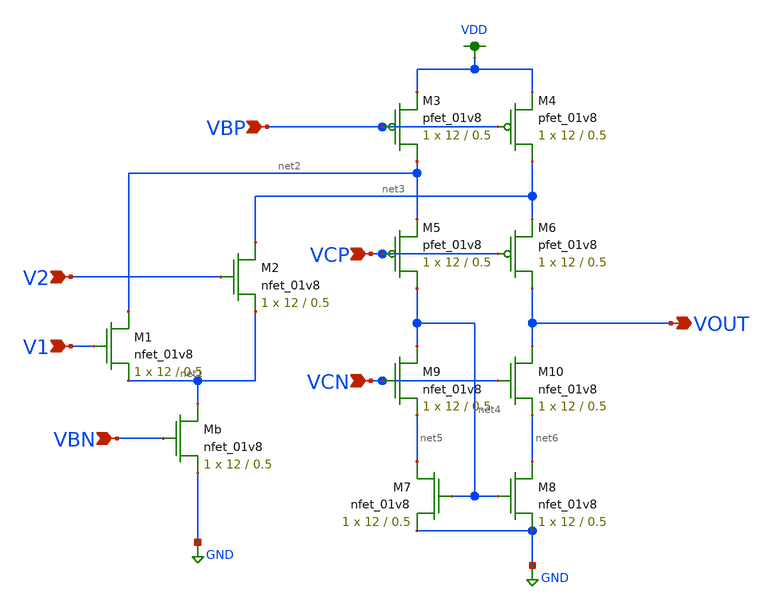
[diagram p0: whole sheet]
** sch_path: MP3/FCDA (copy).sch
**.subckt FCDA (copy) V2 V1 VBN VCN VCP VBP VOUT
*.ipin V2
*.ipin V1
*.ipin VBN
*.ipin VCN
*.ipin VCP
*.ipin VBP
*.opin VOUT
XM1 net2 V1 net1 GND sky130_fd_pr__nfet_01v8 L=0.5 W=12 nf=1 ad='int((nf+1)/2) * W/nf * 0.29' as='int((nf+2)/2) * W/nf * 0.29'
+ pd='2*int((nf+1)/2) * (W/nf + 0.29)' ps='2*int((nf+2)/2) * (W/nf + 0.29)' nrd='0.29 / W' nrs='0.29 / W'
+ sa=0 sb=0 sd=0 mult=1 m=1
XM2 net3 V2 net1 GND sky130_fd_pr__nfet_01v8 L=0.5 W=12 nf=1 ad='int((nf+1)/2) * W/nf * 0.29' as='int((nf+2)/2) * W/nf * 0.29'
+ pd='2*int((nf+1)/2) * (W/nf + 0.29)' ps='2*int((nf+2)/2) * (W/nf + 0.29)' nrd='0.29 / W' nrs='0.29 / W'
+ sa=0 sb=0 sd=0 mult=1 m=1
XM3 net2 VBP VDD VDD sky130_fd_pr__pfet_01v8 L=0.5 W=12 nf=1 ad='int((nf+1)/2) * W/nf * 0.29' as='int((nf+2)/2) * W/nf * 0.29'
+ pd='2*int((nf+1)/2) * (W/nf + 0.29)' ps='2*int((nf+2)/2) * (W/nf + 0.29)' nrd='0.29 / W' nrs='0.29 / W'
+ sa=0 sb=0 sd=0 mult=1 m=1
XM4 net3 VBP VDD VDD sky130_fd_pr__pfet_01v8 L=0.5 W=12 nf=1 ad='int((nf+1)/2) * W/nf * 0.29' as='int((nf+2)/2) * W/nf * 0.29'
+ pd='2*int((nf+1)/2) * (W/nf + 0.29)' ps='2*int((nf+2)/2) * (W/nf + 0.29)' nrd='0.29 / W' nrs='0.29 / W'
+ sa=0 sb=0 sd=0 mult=1 m=1
XM5 net4 VCP net2 VDD sky130_fd_pr__pfet_01v8 L=0.5 W=12 nf=1 ad='int((nf+1)/2) * W/nf * 0.29' as='int((nf+2)/2) * W/nf * 0.29'
+ pd='2*int((nf+1)/2) * (W/nf + 0.29)' ps='2*int((nf+2)/2) * (W/nf + 0.29)' nrd='0.29 / W' nrs='0.29 / W'
+ sa=0 sb=0 sd=0 mult=1 m=1
XM6 VOUT VCP net3 VDD sky130_fd_pr__pfet_01v8 L=0.5 W=12 nf=1 ad='int((nf+1)/2) * W/nf * 0.29' as='int((nf+2)/2) * W/nf * 0.29'
+ pd='2*int((nf+1)/2) * (W/nf + 0.29)' ps='2*int((nf+2)/2) * (W/nf + 0.29)' nrd='0.29 / W' nrs='0.29 / W'
+ sa=0 sb=0 sd=0 mult=1 m=1
XM7 net5 net4 GND GND sky130_fd_pr__nfet_01v8 L=0.5 W=12 nf=1 ad='int((nf+1)/2) * W/nf * 0.29' as='int((nf+2)/2) * W/nf * 0.29'
+ pd='2*int((nf+1)/2) * (W/nf + 0.29)' ps='2*int((nf+2)/2) * (W/nf + 0.29)' nrd='0.29 / W' nrs='0.29 / W'
+ sa=0 sb=0 sd=0 mult=1 m=1
XM8 net6 net4 GND GND sky130_fd_pr__nfet_01v8 L=0.5 W=12 nf=1 ad='int((nf+1)/2) * W/nf * 0.29' as='int((nf+2)/2) * W/nf * 0.29'
+ pd='2*int((nf+1)/2) * (W/nf + 0.29)' ps='2*int((nf+2)/2) * (W/nf + 0.29)' nrd='0.29 / W' nrs='0.29 / W'
+ sa=0 sb=0 sd=0 mult=1 m=1
XM9 net4 VCN net5 GND sky130_fd_pr__nfet_01v8 L=0.5 W=12 nf=1 ad='int((nf+1)/2) * W/nf * 0.29' as='int((nf+2)/2) * W/nf * 0.29'
+ pd='2*int((nf+1)/2) * (W/nf + 0.29)' ps='2*int((nf+2)/2) * (W/nf + 0.29)' nrd='0.29 / W' nrs='0.29 / W'
+ sa=0 sb=0 sd=0 mult=1 m=1
XM10 VOUT VCN net6 GND sky130_fd_pr__nfet_01v8 L=0.5 W=12 nf=1 ad='int((nf+1)/2) * W/nf * 0.29' as='int((nf+2)/2) * W/nf * 0.29'
+ pd='2*int((nf+1)/2) * (W/nf + 0.29)' ps='2*int((nf+2)/2) * (W/nf + 0.29)' nrd='0.29 / W' nrs='0.29 / W'
+ sa=0 sb=0 sd=0 mult=1 m=1
XMb net1 VBN GND GND sky130_fd_pr__nfet_01v8 L=0.5 W=12 nf=1 ad='int((nf+1)/2) * W/nf * 0.29' as='int((nf+2)/2) * W/nf * 0.29'
+ pd='2*int((nf+1)/2) * (W/nf + 0.29)' ps='2*int((nf+2)/2) * (W/nf + 0.29)' nrd='0.29 / W' nrs='0.29 / W'
+ sa=0 sb=0 sd=0 mult=1 m=1
**.ends
.GLOBAL GND
.GLOBAL VDD
.end
